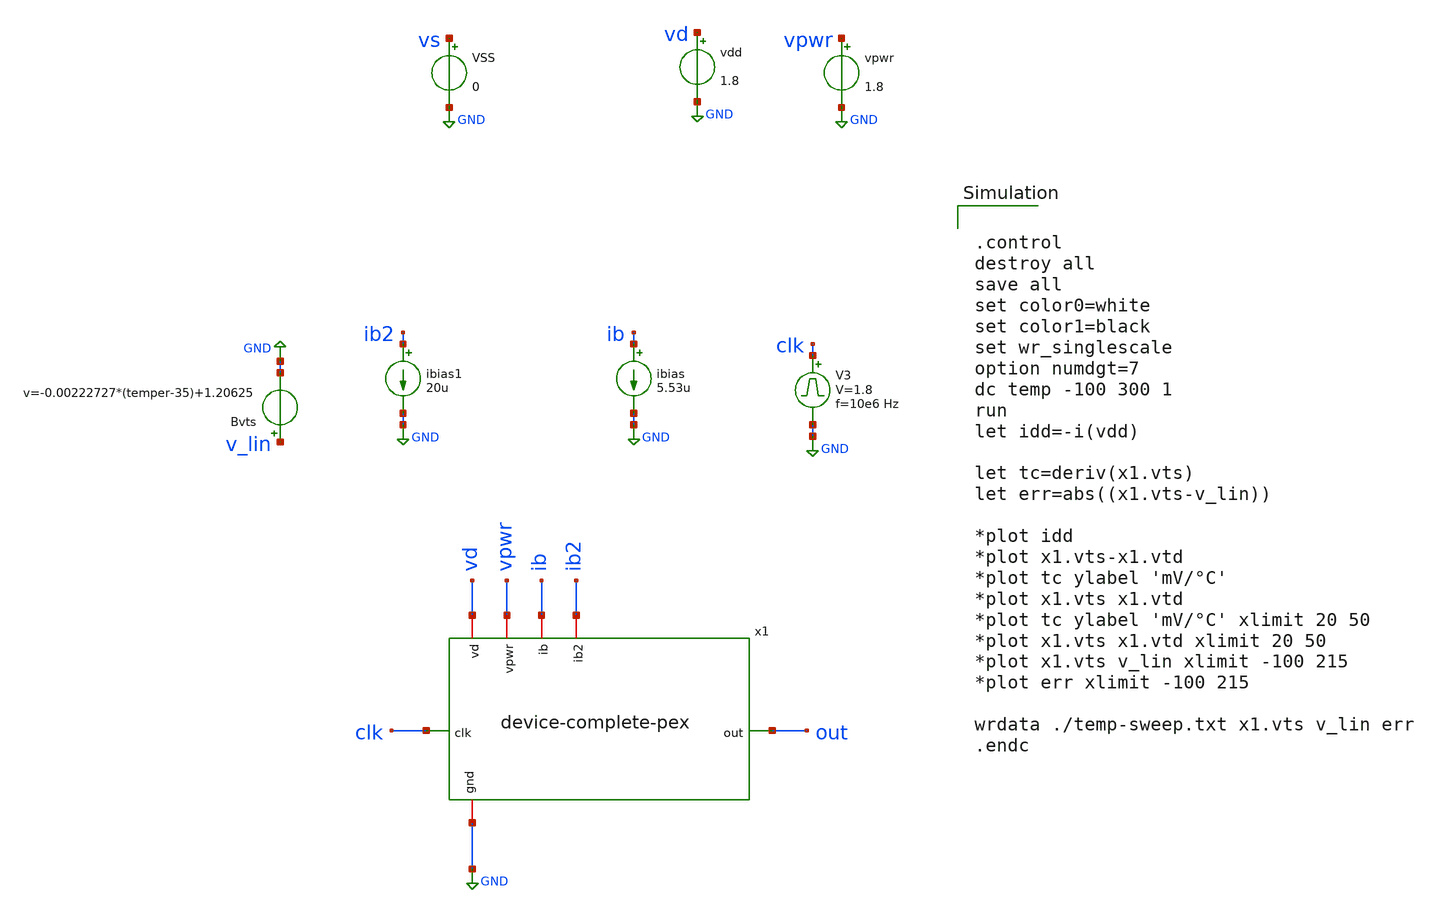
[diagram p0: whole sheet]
** sch_path: device-complete/xschem/device-complete_temp-tb .sch
**.subckt device-complete_temp-tb
vpwr vpwr GND 1.8
V3 clk GND pulse 0 1.8 '0.495/ 10e6 ' '0.01/10e6 ' '0.01/10e6 ' '0.49/10e6 ' '1/10e6 '
vdd vd GND 1.8
ibias ib GND 5.53u
VSS vs GND 0
ibias1 ib2 GND 20u
Bvts v_lin GND v=-0.00222727*(temper-35)+1.20625
x1 vd clk out vpwr ib ib2 GND device-complete-pex
**** begin user architecture code
 .lib $::SKYWATER_MODELS/sky130.lib.spice tt
.include $::SKYWATER_STDCELLS/sky130_fd_sc_hd.spice



.control
destroy all
save all
set color0=white
set color1=black
set wr_singlescale
option numdgt=7
dc temp -100 300 1
run
let idd=-i(vdd)

let tc=deriv(x1.vts)
let err=abs((x1.vts-v_lin))

*plot idd
*plot x1.vts-x1.vtd
*plot tc ylabel 'mV/°C'
*plot x1.vts x1.vtd
*plot tc ylabel 'mV/°C' xlimit 20 50
*plot x1.vts x1.vtd xlimit 20 50
*plot x1.vts v_lin xlimit -100 215
*plot err xlimit -100 215

wrdata ./temp-sweep.txt x1.vts v_lin err
.endc


**** end user architecture code
**.ends
.GLOBAL GND
.end
